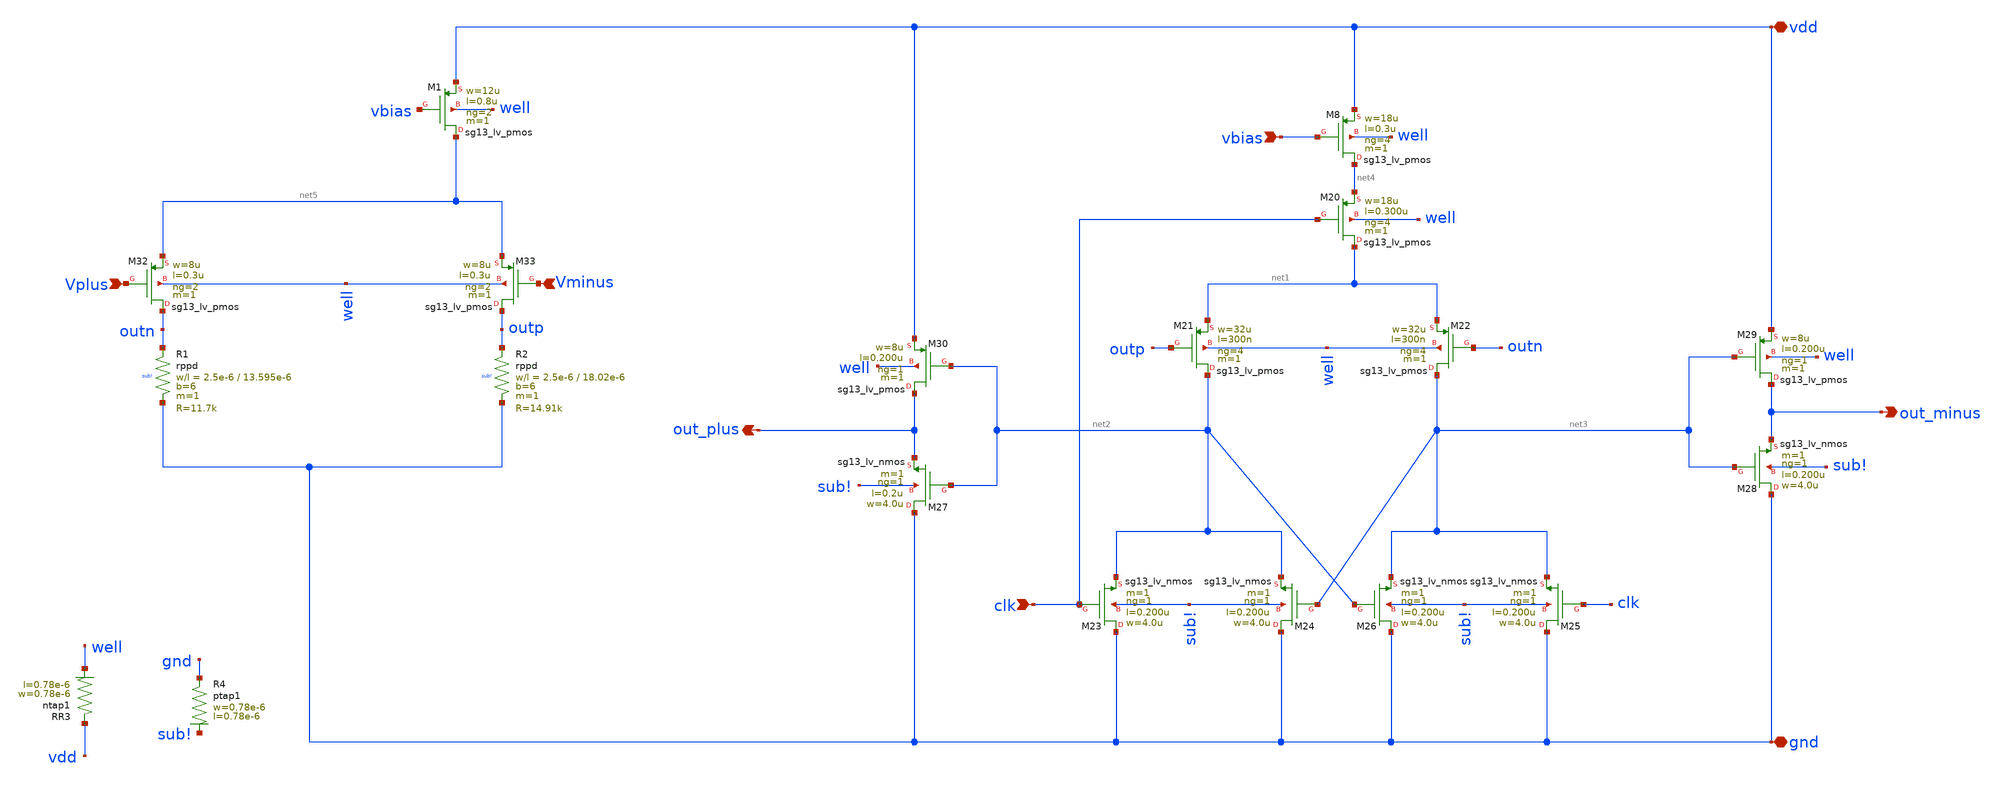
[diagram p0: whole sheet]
** sch_path: schematic/dynamic_comparator_new.sch
**.subckt dynamic_comparator_new vbias out_plus out_minus gnd vdd Vplus Vminus clk
*.ipin vbias
*.opin out_plus
*.opin out_minus
*.iopin gnd
*.iopin vdd
*.ipin Vplus
*.ipin Vminus
*.ipin clk
XM8 net4 vbias vdd well sg13_lv_pmos w=18u l=0.3u ng=4 m=1 mm_ok=1
XM20 net1 clk net4 well sg13_lv_pmos w=18u l=0.300u ng=4 m=1 mm_ok=1
XM21 net2 outp net1 well sg13_lv_pmos w=32u l=300n ng=4 m=1 mm_ok=1
XM22 net3 outn net1 well sg13_lv_pmos w=32u l=300n ng=4 m=1 mm_ok=1
XM23 gnd clk net2 sub! sg13_lv_nmos w=4.0u l=0.200u ng=1 m=1 mm_ok=1
XM24 gnd net3 net2 sub! sg13_lv_nmos w=4.0u l=0.200u ng=1 m=1 mm_ok=1
XM25 gnd clk net3 sub! sg13_lv_nmos w=4.0u l=0.200u ng=1 m=1 mm_ok=1
XM26 gnd net2 net3 sub! sg13_lv_nmos w=4.0u l=0.200u ng=1 m=1 mm_ok=1
XM27 gnd net2 out_plus sub! sg13_lv_nmos w=4.0u l=0.2u ng=1 m=1 mm_ok=1
XM28 gnd net3 out_minus sub! sg13_lv_nmos w=4.0u l=0.200u ng=1 m=1 mm_ok=1
XM29 out_minus net3 vdd well sg13_lv_pmos w=8u l=0.200u ng=1 m=1 mm_ok=1
XM30 out_plus net2 vdd well sg13_lv_pmos w=8u l=0.200u ng=1 m=1 mm_ok=1
XM32 outn Vplus net5 well sg13_lv_pmos w=8u l=0.3u ng=2 m=1 mm_ok=1
XM33 outp Vminus net5 well sg13_lv_pmos w=8u l=0.3u ng=2 m=1 mm_ok=1
XM1 net5 vbias vdd well sg13_lv_pmos w=12u l=0.8u ng=2 m=1 mm_ok=1
XR1 outn gnd sub! rppd w=2.5e-6 l=13.595e-6 m=1 b=6 mm_ok=1
XR2 outp gnd sub! rppd w=2.5e-6 l=18.02e-6 m=1 b=6 mm_ok=1
XR3 vdd well ntap1 R=262.8 w=0.78e-6 l=0.78e-6
XR4 gnd sub! ptap1 R=262.8 w=0.78e-6 l=0.78e-6
**.ends
.end
